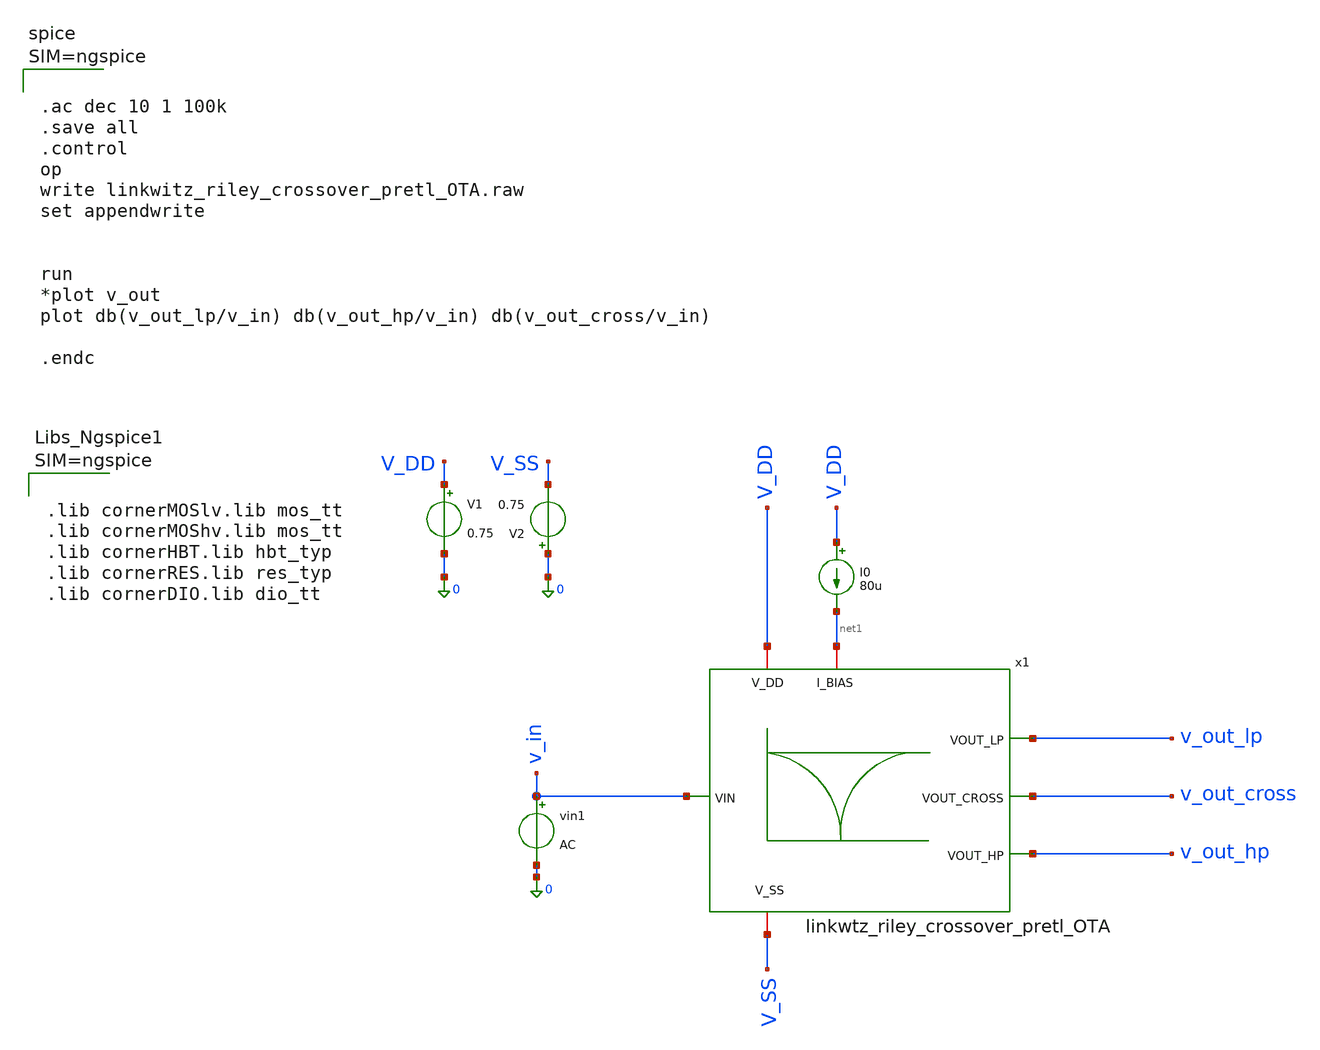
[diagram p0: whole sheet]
** sch_path: 004_Real_Circuits/003_version_second_output_stage/linkwitz_riley_real_circuit_pretl_top_tb.sch
**.subckt linkwitz_riley_real_circuit_pretl_top_tb
I0 V_DD net1 80u
V1 V_DD 0 0.75
vin1 v_in 0 AC
V2 0 V_SS 0.75
x1 v_out_lp net1 V_DD v_out_cross V_SS v_in v_out_hp linkwtz_riley_crossover_pretl_OTA
**** begin user architecture code



.lib cornerMOSlv.lib mos_tt
.lib cornerMOShv.lib mos_tt
.lib cornerHBT.lib hbt_typ
.lib cornerRES.lib res_typ
.lib cornerDIO.lib dio_tt






.ac dec 10 1 100k
.save all
.control
op
write linkwitz_riley_crossover_pretl_OTA.raw
set appendwrite


run
*plot v_out
plot db(v_out_lp/v_in) db(v_out_hp/v_in) db(v_out_cross/v_in)

.endc



**** end user architecture code
**.ends
.end
